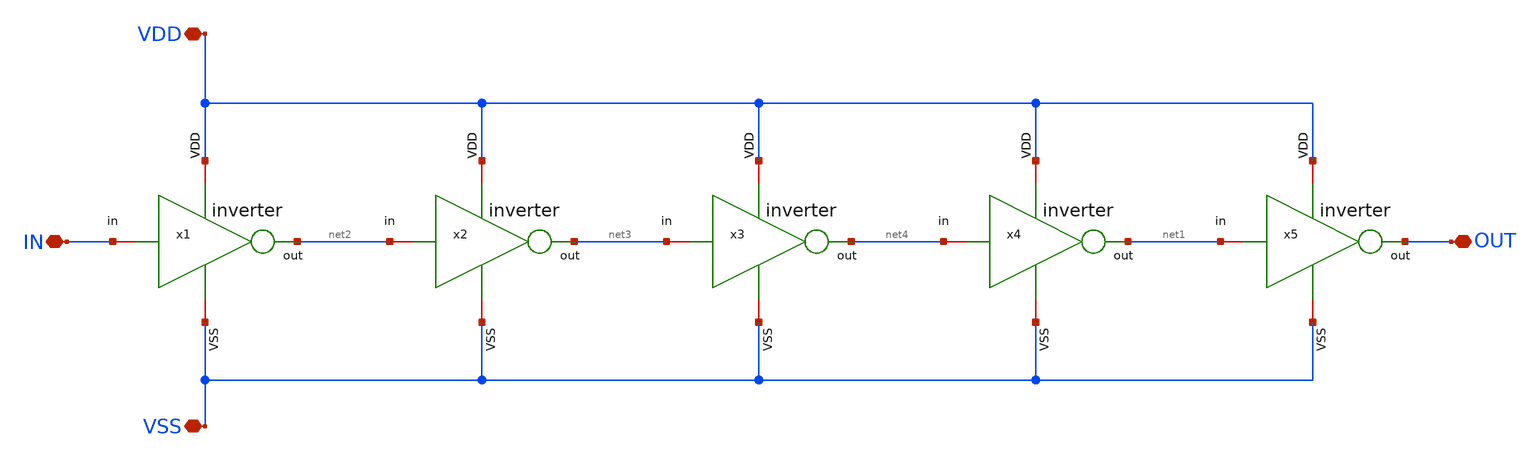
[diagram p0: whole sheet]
** sch_path: designs/sar_adc/digital/delay_cell/xschem/delay_cell_x1.sch
**.subckt delay_cell_x1 IN OUT VDD VSS
*.iopin IN
*.iopin OUT
*.iopin VDD
*.iopin VSS
x1 VDD IN net2 VSS inverter
x2 VDD net2 net3 VSS inverter
x3 VDD net3 net4 VSS inverter
x4 VDD net4 net1 VSS inverter
x5 VDD net1 OUT VSS inverter
**.ends

* expanding   symbol:  designs/sar_adc/digital/edge_inv_x1/xschem/inverter.sym # of pins=6
** sym_path: designs/sar_adc/digital/inverter/xschem/inverter.sym
** sch_path: designs/sar_adc/digital/inverter/xschem/inverter.sch
.subckt inverter VDD in out VSS
*.opin out
*.iopin in
*.iopin VDD
*.iopin VSS
XM1 out in VSS VSS nfet_03v3 L=0.28u W=1u nf=1 ad='int((nf+1)/2) * W/nf * 0.18u' as='int((nf+2)/2) * W/nf * 0.18u'
+ pd='2*int((nf+1)/2) * (W/nf + 0.18u)' ps='2*int((nf+2)/2) * (W/nf + 0.18u)' nrd='0.18u / W' nrs='0.18u / W'
+ sa=0 sb=0 sd=0 m=1
XM2 out in VDD VDD pfet_03v3 L=0.28u W=3u nf=1 ad='int((nf+1)/2) * W/nf * 0.18u' as='int((nf+2)/2) * W/nf * 0.18u'
+ pd='2*int((nf+1)/2) * (W/nf + 0.18u)' ps='2*int((nf+2)/2) * (W/nf + 0.18u)' nrd='0.18u / W' nrs='0.18u / W'
+ sa=0 sb=0 sd=0 m=1
.ends

.end
